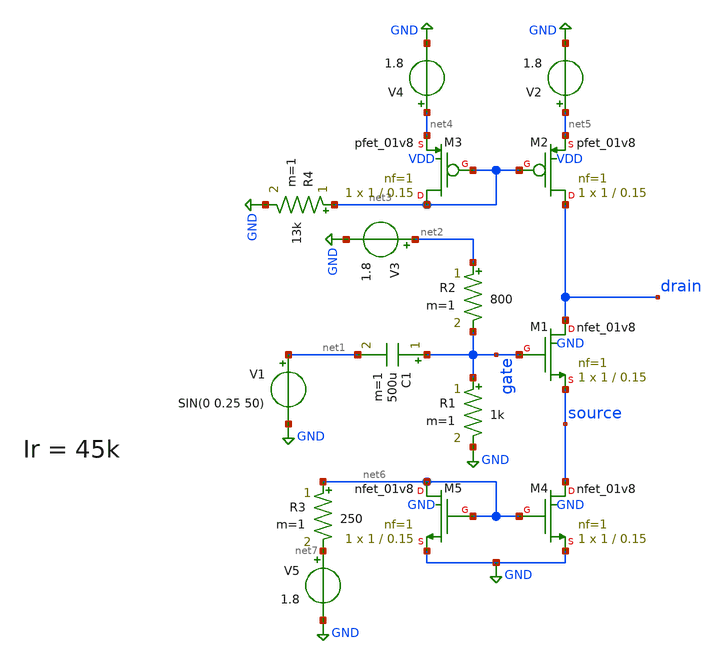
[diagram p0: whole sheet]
** sch_path: xschem/untitled-3.sch
**.subckt untitled-3
XM1 drain gate source GND sky130_fd_pr__nfet_01v8 L=0.15 W=1 nf=1 ad='int((nf+1)/2) * W/nf * 0.29' as='int((nf+2)/2) * W/nf * 0.29'
+ pd='2*int((nf+1)/2) * (W/nf + 0.29)' ps='2*int((nf+2)/2) * (W/nf + 0.29)' nrd='0.29 / W' nrs='0.29 / W'
+ sa=0 sb=0 sd=0 mult=1 m=1
V1 net1 GND SIN(0 0.25 50)
C1 gate net1 500u m=1
R1 gate GND 1k m=1
R2 net2 gate 800 m=1
V3 net2 GND 1.8
XM2 drain net3 net5 VDD sky130_fd_pr__pfet_01v8 L=0.15 W=1 nf=1 ad='int((nf+1)/2) * W/nf * 0.29' as='int((nf+2)/2) * W/nf * 0.29'
+ pd='2*int((nf+1)/2) * (W/nf + 0.29)' ps='2*int((nf+2)/2) * (W/nf + 0.29)' nrd='0.29 / W' nrs='0.29 / W'
+ sa=0 sb=0 sd=0 mult=1 m=1
XM3 net3 net3 net4 VDD sky130_fd_pr__pfet_01v8 L=0.15 W=1 nf=1 ad='int((nf+1)/2) * W/nf * 0.29' as='int((nf+2)/2) * W/nf * 0.29'
+ pd='2*int((nf+1)/2) * (W/nf + 0.29)' ps='2*int((nf+2)/2) * (W/nf + 0.29)' nrd='0.29 / W' nrs='0.29 / W'
+ sa=0 sb=0 sd=0 mult=1 m=1
V2 net5 GND 1.8
V4 net4 GND 1.8
R4 net3 GND 13k m=1
XM4 source net6 GND GND sky130_fd_pr__nfet_01v8 L=0.15 W=1 nf=1 ad='int((nf+1)/2) * W/nf * 0.29' as='int((nf+2)/2) * W/nf * 0.29'
+ pd='2*int((nf+1)/2) * (W/nf + 0.29)' ps='2*int((nf+2)/2) * (W/nf + 0.29)' nrd='0.29 / W' nrs='0.29 / W'
+ sa=0 sb=0 sd=0 mult=1 m=1
XM5 net6 net6 GND GND sky130_fd_pr__nfet_01v8 L=0.15 W=1 nf=1 ad='int((nf+1)/2) * W/nf * 0.29' as='int((nf+2)/2) * W/nf * 0.29'
+ pd='2*int((nf+1)/2) * (W/nf + 0.29)' ps='2*int((nf+2)/2) * (W/nf + 0.29)' nrd='0.29 / W' nrs='0.29 / W'
+ sa=0 sb=0 sd=0 mult=1 m=1
R3 net6 net7 250 m=1
V5 net7 GND 1.8
**** begin user architecture code
 ** manual skywater pdks install (with patches applied)
* .lib $::SKYWATER_MODELS/models/sky130.lib.spice tt

** opencircuitdesign pdks install
.lib $::SKYWATER_MODELS/sky130.lib.spice tt

.param mc_mm_switch=0
.param mc_pr_switch=0



.tran 0.001s 0.1
.control
  run
  plot v(drain) v(gate)
.endc
.save all


**** end user architecture code
**.ends
.GLOBAL GND
.end
